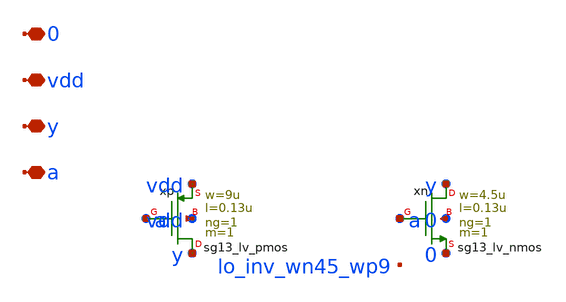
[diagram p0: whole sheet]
** sch_path: analog/lo/sch/lo_inv_45_9.sch
**.subckt lo_inv_45_9 a y vdd 0
*.iopin a
*.iopin y
*.iopin vdd
*.iopin 0
Xxp y a vdd vdd sg13_lv_pmos w=9u l=0.13u ng=1 m=1 mm_ok=1
Xxn y a 0 0 sg13_lv_nmos w=4.5u l=0.13u ng=1 m=1 mm_ok=1
**.ends
.end
